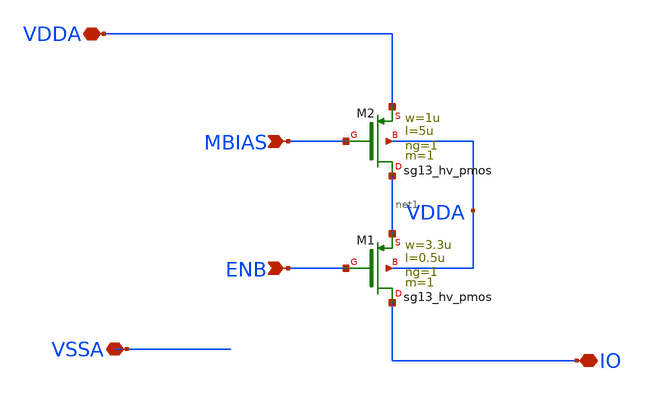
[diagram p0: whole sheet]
** sch_path: ISOURCE.sch
**.subckt ISOURCE VDDA MBIAS ENB IO VSSA
*.iopin VDDA
*.ipin MBIAS
*.ipin ENB
*.iopin IO
*.iopin VSSA
XM2 net1 MBIAS VDDA VDDA sg13_hv_pmos w=1u l=5u ng=1 m=1 mm_ok=1
XM1 IO ENB net1 VDDA sg13_hv_pmos w=3.3u l=0.5u ng=1 m=1 mm_ok=1
**.ends
.end
